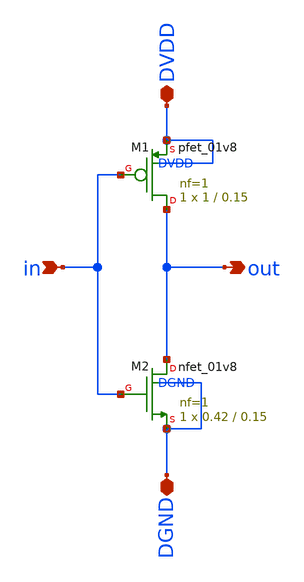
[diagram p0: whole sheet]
** sch_path: tutorials/tutorial_4/inv.sch
**.subckt inv out in DGND DVDD
*.opin out
*.ipin in
*.iopin DGND
*.iopin DVDD
XM2 out in DGND DGND sky130_fd_pr__nfet_01v8 L=0.15 W=0.42 nf=1 ad='int((nf+1)/2) * W/nf * 0.29' as='int((nf+2)/2) * W/nf * 0.29'
+ pd='2*int((nf+1)/2) * (W/nf + 0.29)' ps='2*int((nf+2)/2) * (W/nf + 0.29)' nrd='0.29 / W' nrs='0.29 / W'
+ sa=0 sb=0 sd=0 mult=1 m=1
XM1 out in DVDD DVDD sky130_fd_pr__pfet_01v8 L=0.15 W=1 nf=1 ad='int((nf+1)/2) * W/nf * 0.29' as='int((nf+2)/2) * W/nf * 0.29'
+ pd='2*int((nf+1)/2) * (W/nf + 0.29)' ps='2*int((nf+2)/2) * (W/nf + 0.29)' nrd='0.29 / W' nrs='0.29 / W'
+ sa=0 sb=0 sd=0 mult=1 m=1
**.ends
.end
